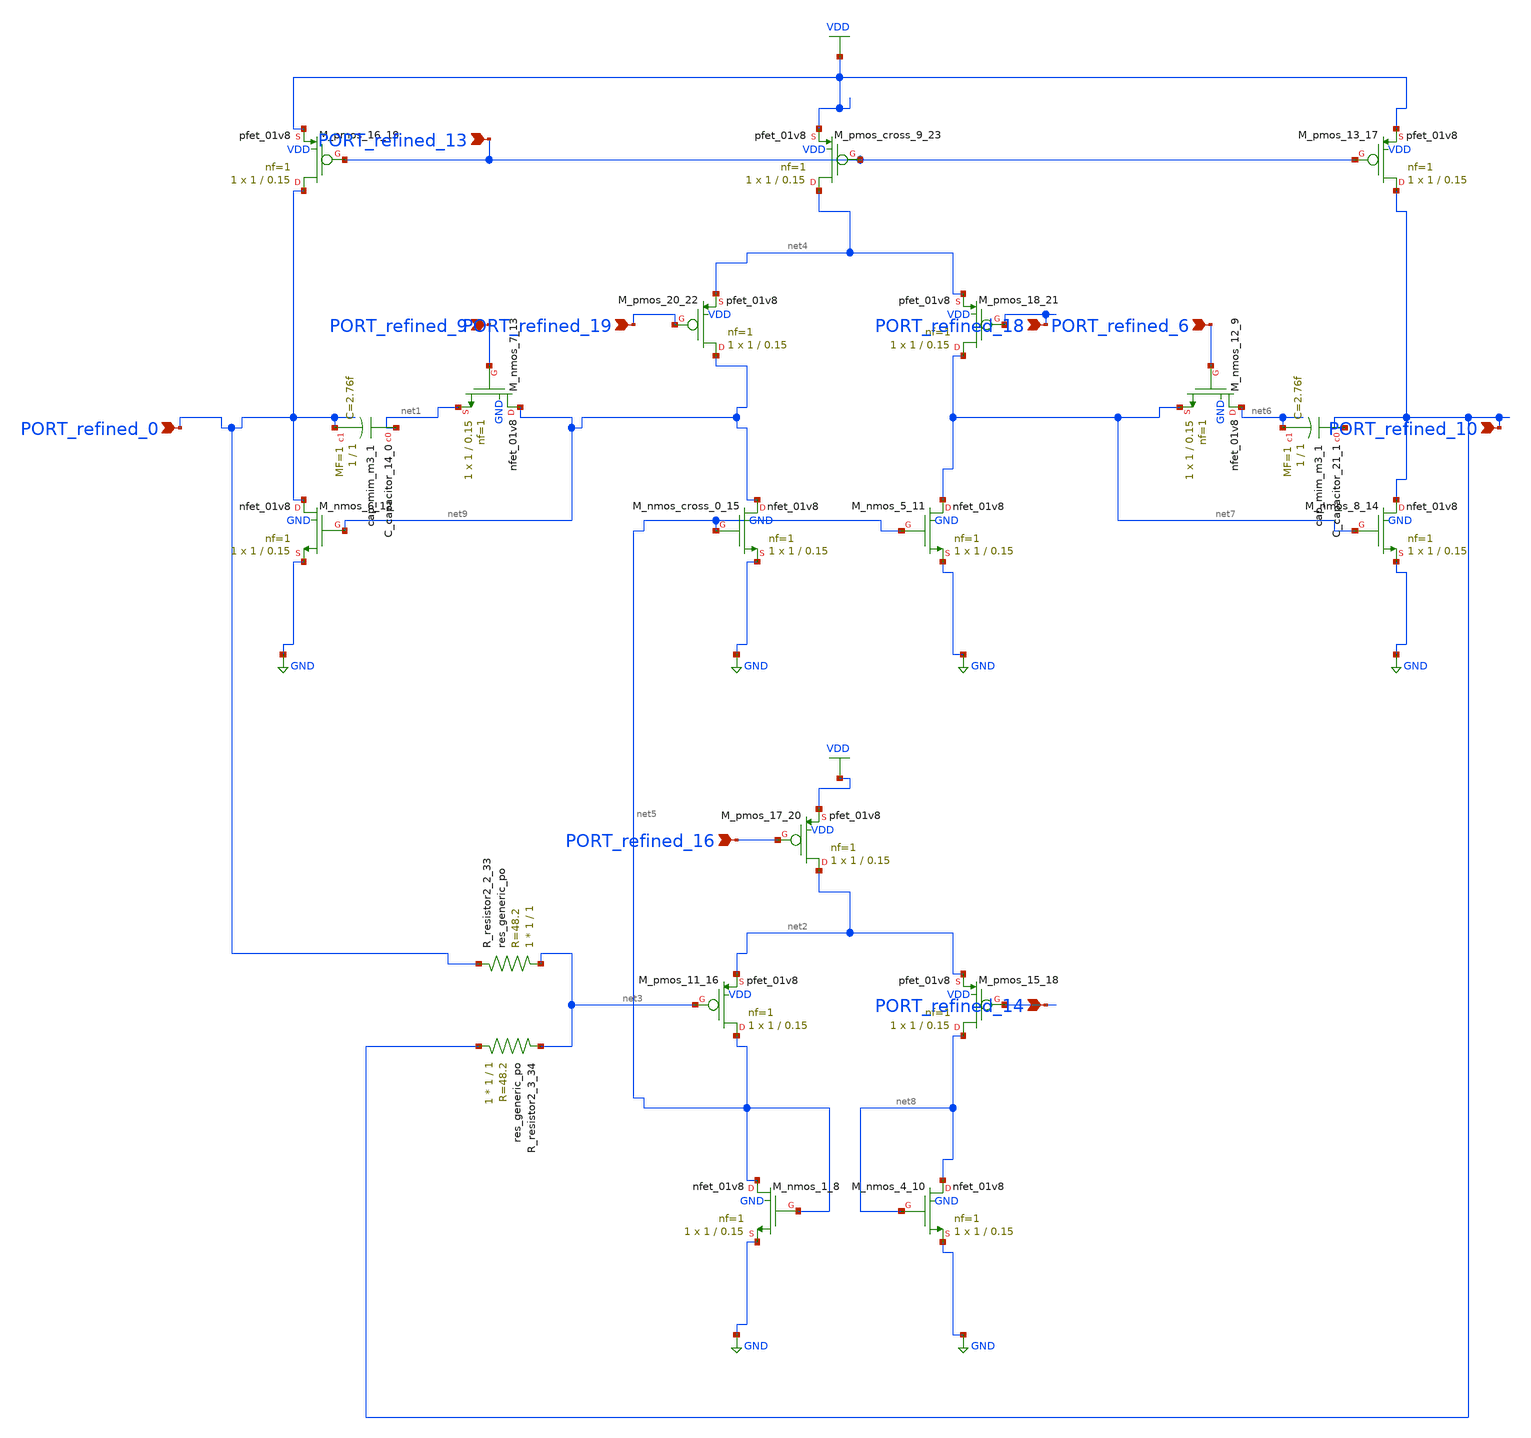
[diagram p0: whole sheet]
** sch_path: schematics/Image2Net/063.sch
**.subckt 063 PORT_refined_10 PORT_refined_14 PORT_refined_13 PORT_refined_16 PORT_refined_6
*+ PORT_refined_9 PORT_refined_0 PORT_refined_19 PORT_refined_18
*.ipin PORT_refined_10
*.ipin PORT_refined_14
*.ipin PORT_refined_13
*.ipin PORT_refined_16
*.ipin PORT_refined_6
*.ipin PORT_refined_9
*.ipin PORT_refined_0
*.ipin PORT_refined_19
*.ipin PORT_refined_18
XC_capacitor_14_0 net1 PORT_refined_0 sky130_fd_pr__cap_mim_m3_1 W=1 L=1 MF=1 m=1
XC_capacitor_21_1 PORT_refined_10 net6 sky130_fd_pr__cap_mim_m3_1 W=1 L=1 MF=1 m=1
XM_nmos_1_8 net5 net5 GND GND sky130_fd_pr__nfet_01v8 L=0.15 W=1 nf=1 ad='int((1 + 1)/2) * 1 / 1 * 0.29'
+ as='int((1 + 2)/2) * 1 / 1 * 0.29' pd='2*int((1 + 1)/2) * (1 / 1 + 0.29)' ps='2*int((1 + 2)/2) * (1 / 1 + 0.29)'
+ nrd='0.29 / 1 ' nrs='0.29 / 1 ' sa=0 sb=0 sd=0 mult=1 m=1
XM_nmos_12_9 net6 PORT_refined_6 net7 GND sky130_fd_pr__nfet_01v8 L=0.15 W=1 nf=1 ad='int((1 + 1)/2) * 1 / 1 * 0.29'
+ as='int((1 + 2)/2) * 1 / 1 * 0.29' pd='2*int((1 + 1)/2) * (1 / 1 + 0.29)' ps='2*int((1 + 2)/2) * (1 / 1 + 0.29)'
+ nrd='0.29 / 1 ' nrs='0.29 / 1 ' sa=0 sb=0 sd=0 mult=1 m=1
XM_nmos_4_10 net8 net8 GND GND sky130_fd_pr__nfet_01v8 L=0.15 W=1 nf=1 ad='int((1 + 1)/2) * 1 / 1 * 0.29'
+ as='int((1 + 2)/2) * 1 / 1 * 0.29' pd='2*int((1 + 1)/2) * (1 / 1 + 0.29)' ps='2*int((1 + 2)/2) * (1 / 1 + 0.29)'
+ nrd='0.29 / 1 ' nrs='0.29 / 1 ' sa=0 sb=0 sd=0 mult=1 m=1
XM_nmos_5_11 net7 net5 GND GND sky130_fd_pr__nfet_01v8 L=0.15 W=1 nf=1 ad='int((1 + 1)/2) * 1 / 1 * 0.29'
+ as='int((1 + 2)/2) * 1 / 1 * 0.29' pd='2*int((1 + 1)/2) * (1 / 1 + 0.29)' ps='2*int((1 + 2)/2) * (1 / 1 + 0.29)'
+ nrd='0.29 / 1 ' nrs='0.29 / 1 ' sa=0 sb=0 sd=0 mult=1 m=1
XM_nmos_6_12 PORT_refined_0 net9 GND GND sky130_fd_pr__nfet_01v8 L=0.15 W=1 nf=1 ad='int((1 + 1)/2) * 1 / 1 * 0.29'
+ as='int((1 + 2)/2) * 1 / 1 * 0.29' pd='2*int((1 + 1)/2) * (1 / 1 + 0.29)' ps='2*int((1 + 2)/2) * (1 / 1 + 0.29)'
+ nrd='0.29 / 1 ' nrs='0.29 / 1 ' sa=0 sb=0 sd=0 mult=1 m=1
XM_nmos_7_13 net9 PORT_refined_9 net1 GND sky130_fd_pr__nfet_01v8 L=0.15 W=1 nf=1 ad='int((1 + 1)/2) * 1 / 1 * 0.29'
+ as='int((1 + 2)/2) * 1 / 1 * 0.29' pd='2*int((1 + 1)/2) * (1 / 1 + 0.29)' ps='2*int((1 + 2)/2) * (1 / 1 + 0.29)'
+ nrd='0.29 / 1 ' nrs='0.29 / 1 ' sa=0 sb=0 sd=0 mult=1 m=1
XM_nmos_8_14 PORT_refined_10 net7 GND GND sky130_fd_pr__nfet_01v8 L=0.15 W=1 nf=1 ad='int((1 + 1)/2) * 1 / 1 * 0.29'
+ as='int((1 + 2)/2) * 1 / 1 * 0.29' pd='2*int((1 + 1)/2) * (1 / 1 + 0.29)' ps='2*int((1 + 2)/2) * (1 / 1 + 0.29)'
+ nrd='0.29 / 1 ' nrs='0.29 / 1 ' sa=0 sb=0 sd=0 mult=1 m=1
XM_nmos_cross_0_15 net9 net5 GND GND sky130_fd_pr__nfet_01v8 L=0.15 W=1 nf=1 ad='int((1 + 1)/2) * 1 / 1 * 0.29'
+ as='int((1 + 2)/2) * 1 / 1 * 0.29' pd='2*int((1 + 1)/2) * (1 / 1 + 0.29)' ps='2*int((1 + 2)/2) * (1 / 1 + 0.29)'
+ nrd='0.29 / 1 ' nrs='0.29 / 1 ' sa=0 sb=0 sd=0 mult=1 m=1
XM_pmos_11_16 net5 net3 net2 VDD sky130_fd_pr__pfet_01v8 L=0.15 W=1 nf=1 ad='int((1 + 1)/2) * 1 / 1 * 0.29'
+ as='int((1 + 2)/2) * 1 / 1 * 0.29' pd='2*int((1 + 1)/2) * (1 / 1 + 0.29)' ps='2*int((1 + 2)/2) * (1 / 1 + 0.29)'
+ nrd='0.29 / 1 ' nrs='0.29 / 1 ' sa=0 sb=0 sd=0 mult=1 m=1
XM_pmos_13_17 PORT_refined_10 PORT_refined_13 VDD VDD sky130_fd_pr__pfet_01v8 L=0.15 W=1 nf=1 ad='int((1 + 1)/2) * 1 / 1 * 0.29'
+ as='int((1 + 2)/2) * 1 / 1 * 0.29' pd='2*int((1 + 1)/2) * (1 / 1 + 0.29)' ps='2*int((1 + 2)/2) * (1 / 1 + 0.29)'
+ nrd='0.29 / 1 ' nrs='0.29 / 1 ' sa=0 sb=0 sd=0 mult=1 m=1
XM_pmos_15_18 net8 PORT_refined_14 net2 VDD sky130_fd_pr__pfet_01v8 L=0.15 W=1 nf=1 ad='int((1 + 1)/2) * 1 / 1 * 0.29'
+ as='int((1 + 2)/2) * 1 / 1 * 0.29' pd='2*int((1 + 1)/2) * (1 / 1 + 0.29)' ps='2*int((1 + 2)/2) * (1 / 1 + 0.29)'
+ nrd='0.29 / 1 ' nrs='0.29 / 1 ' sa=0 sb=0 sd=0 mult=1 m=1
XM_pmos_16_19 PORT_refined_0 PORT_refined_13 VDD VDD sky130_fd_pr__pfet_01v8 L=0.15 W=1 nf=1 ad='int((1 + 1)/2) * 1 / 1 * 0.29'
+ as='int((1 + 2)/2) * 1 / 1 * 0.29' pd='2*int((1 + 1)/2) * (1 / 1 + 0.29)' ps='2*int((1 + 2)/2) * (1 / 1 + 0.29)'
+ nrd='0.29 / 1 ' nrs='0.29 / 1 ' sa=0 sb=0 sd=0 mult=1 m=1
XM_pmos_17_20 net2 PORT_refined_16 VDD VDD sky130_fd_pr__pfet_01v8 L=0.15 W=1 nf=1 ad='int((1 + 1)/2) * 1 / 1 * 0.29'
+ as='int((1 + 2)/2) * 1 / 1 * 0.29' pd='2*int((1 + 1)/2) * (1 / 1 + 0.29)' ps='2*int((1 + 2)/2) * (1 / 1 + 0.29)'
+ nrd='0.29 / 1 ' nrs='0.29 / 1 ' sa=0 sb=0 sd=0 mult=1 m=1
XM_pmos_18_21 net7 PORT_refined_18 net4 VDD sky130_fd_pr__pfet_01v8 L=0.15 W=1 nf=1 ad='int((1 + 1)/2) * 1 / 1 * 0.29'
+ as='int((1 + 2)/2) * 1 / 1 * 0.29' pd='2*int((1 + 1)/2) * (1 / 1 + 0.29)' ps='2*int((1 + 2)/2) * (1 / 1 + 0.29)'
+ nrd='0.29 / 1 ' nrs='0.29 / 1 ' sa=0 sb=0 sd=0 mult=1 m=1
XM_pmos_20_22 net9 PORT_refined_19 net4 VDD sky130_fd_pr__pfet_01v8 L=0.15 W=1 nf=1 ad='int((1 + 1)/2) * 1 / 1 * 0.29'
+ as='int((1 + 2)/2) * 1 / 1 * 0.29' pd='2*int((1 + 1)/2) * (1 / 1 + 0.29)' ps='2*int((1 + 2)/2) * (1 / 1 + 0.29)'
+ nrd='0.29 / 1 ' nrs='0.29 / 1 ' sa=0 sb=0 sd=0 mult=1 m=1
XM_pmos_cross_9_23 net4 PORT_refined_13 VDD VDD sky130_fd_pr__pfet_01v8 L=0.15 W=1 nf=1 ad='int((1 + 1)/2) * 1 / 1 * 0.29'
+ as='int((1 + 2)/2) * 1 / 1 * 0.29' pd='2*int((1 + 1)/2) * (1 / 1 + 0.29)' ps='2*int((1 + 2)/2) * (1 / 1 + 0.29)'
+ nrd='0.29 / 1 ' nrs='0.29 / 1 ' sa=0 sb=0 sd=0 mult=1 m=1
XR_resistor2_2_33 net3 PORT_refined_0 sky130_fd_pr__res_generic_po W=1 L=1 m=1
XR_resistor2_3_34 PORT_refined_10 net3 sky130_fd_pr__res_generic_po W=1 L=1 m=1
**.ends
.GLOBAL GND
.GLOBAL VDD
.end
